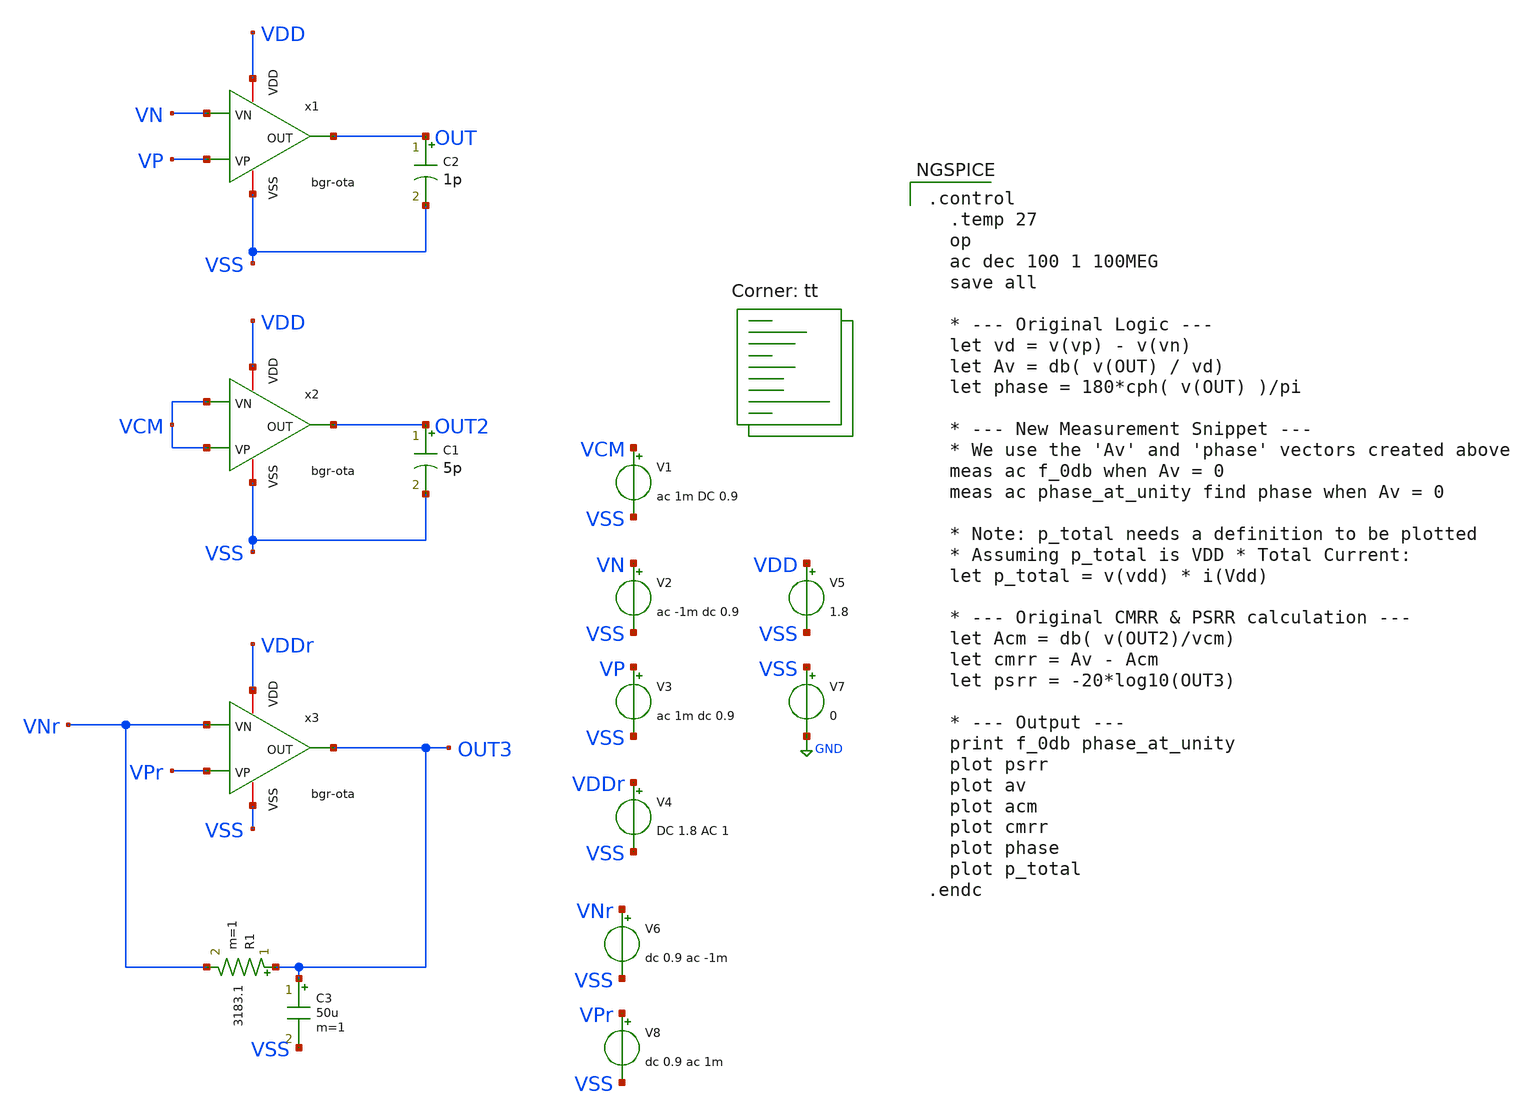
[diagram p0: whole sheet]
** sch_path: xschem/bandgap/bgr_ota/tb_bgr-ota.sch
**.subckt tb_bgr-ota
V2 VN VSS ac -1m dc 0.9
V3 VP VSS ac 1m dc 0.9
V5 VDD VSS 1.8
V7 VSS GND 0
C2 OUT VSS 1p m=1
C1 OUT2 VSS 5p m=1
V1 VCM VSS ac 1m DC 0.9
C3 OUT3 VSS 50u m=1
R1 OUT3 VNr 3183.1 m=1
V4 VDDr VSS DC 1.8 AC 1
x1 VDD OUT VP VN VSS bgr-ota
x2 VDD OUT2 VCM VCM VSS bgr-ota
x3 VDDr OUT3 VPr VNr VSS bgr-ota
V6 VNr VSS dc 0.9 ac -1m
V8 VPr VSS dc 0.9 ac 1m
**** begin user architecture code

.control
  .temp 27
  op
  ac dec 100 1 100MEG
  save all

  * --- Original Logic ---
  let vd = v(vp) - v(vn)
  let Av = db( v(OUT) / vd)
  let phase = 180*cph( v(OUT) )/pi

  * --- New Measurement Snippet ---
  * We use the 'Av' and 'phase' vectors created above
  meas ac f_0db when Av = 0
  meas ac phase_at_unity find phase when Av = 0

  * Note: p_total needs a definition to be plotted
  * Assuming p_total is VDD * Total Current:
  let p_total = v(vdd) * i(Vdd)

  * --- Original CMRR & PSRR calculation ---
  let Acm = db( v(OUT2)/vcm)
  let cmrr = Av - Acm
  let psrr = -20*log10(OUT3)

  * --- Output ---
  print f_0db phase_at_unity
  plot psrr
  plot av
  plot acm
  plot cmrr
  plot phase
  plot p_total
.endc



.lib $::SKYWATER_MODELS/sky130.lib.spice tt
**** end user architecture code
**.ends

* expanding   symbol:  icdec-biomedical-pmic/xschem/bandgap/bgr_ota/bgr-ota.sym # of pins=5
** sym_path: xschem/bandgap/bgr_ota/bgr-ota.sym
** sch_path: xschem/bandgap/bgr_ota/bgr-ota.sch
.subckt bgr-ota VDD OUT VP VN VSS
*.iopin VSS
*.iopin VDD
*.ipin VP
*.ipin VN
*.opin OUT
XM1 net1 VP net3 VSS sky130_fd_pr__nfet_01v8 L=0.3 W=2.5 nf=2 ad='int((nf+1)/2) * W/nf * 0.29' as='int((nf+2)/2) * W/nf * 0.29'
+ pd='2*int((nf+1)/2) * (W/nf + 0.29)' ps='2*int((nf+2)/2) * (W/nf + 0.29)' nrd='0.29 / W' nrs='0.29 / W'
+ sa=0 sb=0 sd=0 mult=1 m=1
XM2 net2 VN net3 VSS sky130_fd_pr__nfet_01v8 L=0.3 W=2.5 nf=2 ad='int((nf+1)/2) * W/nf * 0.29' as='int((nf+2)/2) * W/nf * 0.29'
+ pd='2*int((nf+1)/2) * (W/nf + 0.29)' ps='2*int((nf+2)/2) * (W/nf + 0.29)' nrd='0.29 / W' nrs='0.29 / W'
+ sa=0 sb=0 sd=0 mult=1 m=1
XM4 net2 net1 VDD VDD sky130_fd_pr__pfet_01v8 L=1.25 W=10.8 nf=4 ad='int((nf+1)/2) * W/nf * 0.29' as='int((nf+2)/2) * W/nf * 0.29'
+ pd='2*int((nf+1)/2) * (W/nf + 0.29)' ps='2*int((nf+2)/2) * (W/nf + 0.29)' nrd='0.29 / W' nrs='0.29 / W'
+ sa=0 sb=0 sd=0 mult=1 m=1
XM5 net1 net1 VDD VDD sky130_fd_pr__pfet_01v8 L=1.25 W=10.8 nf=4 ad='int((nf+1)/2) * W/nf * 0.29' as='int((nf+2)/2) * W/nf * 0.29'
+ pd='2*int((nf+1)/2) * (W/nf + 0.29)' ps='2*int((nf+2)/2) * (W/nf + 0.29)' nrd='0.29 / W' nrs='0.29 / W'
+ sa=0 sb=0 sd=0 mult=1 m=1
XM6 net3 IB VSS VSS sky130_fd_pr__nfet_01v8 L=1.25 W=3.4 nf=1 ad='int((nf+1)/2) * W/nf * 0.29' as='int((nf+2)/2) * W/nf * 0.29'
+ pd='2*int((nf+1)/2) * (W/nf + 0.29)' ps='2*int((nf+2)/2) * (W/nf + 0.29)' nrd='0.29 / W' nrs='0.29 / W'
+ sa=0 sb=0 sd=0 mult=1 m=1
XM3 IB net5 net4 net4 sky130_fd_pr__nfet_01v8 L=1.25 W=3.4 nf=1 ad='int((nf+1)/2) * W/nf * 0.29' as='int((nf+2)/2) * W/nf * 0.29'
+ pd='2*int((nf+1)/2) * (W/nf + 0.29)' ps='2*int((nf+2)/2) * (W/nf + 0.29)' nrd='0.29 / W' nrs='0.29 / W'
+ sa=0 sb=0 sd=0 mult=1 m=1
XM7 IB IB VDD VDD sky130_fd_pr__pfet_01v8 L=1.25 W=10.8 nf=4 ad='int((nf+1)/2) * W/nf * 0.29' as='int((nf+2)/2) * W/nf * 0.29'
+ pd='2*int((nf+1)/2) * (W/nf + 0.29)' ps='2*int((nf+2)/2) * (W/nf + 0.29)' nrd='0.29 / W' nrs='0.29 / W'
+ sa=0 sb=0 sd=0 mult=1 m=1
XM8 net5 IB VDD VDD sky130_fd_pr__pfet_01v8 L=1.25 W=10.8 nf=4 ad='int((nf+1)/2) * W/nf * 0.29' as='int((nf+2)/2) * W/nf * 0.29'
+ pd='2*int((nf+1)/2) * (W/nf + 0.29)' ps='2*int((nf+2)/2) * (W/nf + 0.29)' nrd='0.29 / W' nrs='0.29 / W'
+ sa=0 sb=0 sd=0 mult=1 m=1
XM9 net5 net5 VSS VSS sky130_fd_pr__nfet_01v8 L=1.25 W=3.4 nf=1 ad='int((nf+1)/2) * W/nf * 0.29' as='int((nf+2)/2) * W/nf * 0.29'
+ pd='2*int((nf+1)/2) * (W/nf + 0.29)' ps='2*int((nf+2)/2) * (W/nf + 0.29)' nrd='0.29 / W' nrs='0.29 / W'
+ sa=0 sb=0 sd=0 mult=1 m=1
XM11 OUT net2 VDD VDD sky130_fd_pr__pfet_01v8 L=1.25 W=110 nf=32 ad='int((nf+1)/2) * W/nf * 0.29' as='int((nf+2)/2) * W/nf * 0.29'
+ pd='2*int((nf+1)/2) * (W/nf + 0.29)' ps='2*int((nf+2)/2) * (W/nf + 0.29)' nrd='0.29 / W' nrs='0.29 / W'
+ sa=0 sb=0 sd=0 mult=1 m=1
XM12 OUT IB VSS VSS sky130_fd_pr__nfet_01v8 L=1.25 W=10 nf=4 ad='int((nf+1)/2) * W/nf * 0.29' as='int((nf+2)/2) * W/nf * 0.29'
+ pd='2*int((nf+1)/2) * (W/nf + 0.29)' ps='2*int((nf+2)/2) * (W/nf + 0.29)' nrd='0.29 / W' nrs='0.29 / W'
+ sa=0 sb=0 sd=0 mult=1 m=1
XC1 OUT net2 sky130_fd_pr__cap_mim_m3_1 W=20 L=20 MF=4 m=4
XM14 IB IB net5 net5 sky130_fd_pr__nfet_01v8 L=0.15 W=0.85 nf=1 ad='int((nf+1)/2) * W/nf * 0.29' as='int((nf+2)/2) * W/nf * 0.29'
+ pd='2*int((nf+1)/2) * (W/nf + 0.29)' ps='2*int((nf+2)/2) * (W/nf + 0.29)' nrd='0.29 / W' nrs='0.29 / W'
+ sa=0 sb=0 sd=0 mult=1 m=1
XR1 net6 net4 VSS sky130_fd_pr__res_high_po_1p41 L=3.235 mult=1 m=1
XR2 net8 net6 VSS sky130_fd_pr__res_high_po_1p41 L=3.235 mult=1 m=1
XR3 net7 net8 VSS sky130_fd_pr__res_high_po_1p41 L=3.235 mult=1 m=1
XR4 net9 net7 VSS sky130_fd_pr__res_high_po_1p41 L=3.235 mult=1 m=1
XR5 VSS net9 VSS sky130_fd_pr__res_high_po_1p41 L=3.235 mult=1 m=1
.ends

.GLOBAL GND
.end
